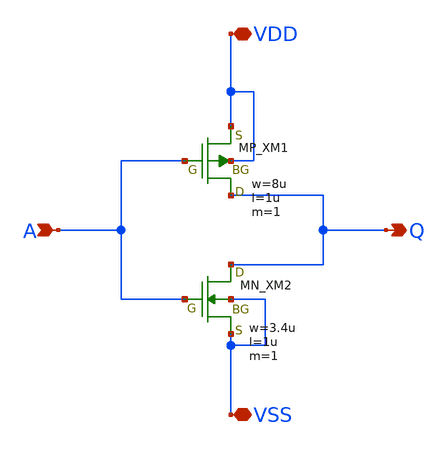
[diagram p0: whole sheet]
** sch_path: inverter/inverter_Tsukasa_Yamamoto.sch
**.subckt inverter_Tsukasa_Yamamoto VDD A Q VSS
*.iopin VDD
*.ipin A
*.opin Q
*.iopin VSS
XXM1 Q A VDD VDD PMOS w=8u l=1u nrd=0 nrs=0 m=1
XXM2 Q A VSS VSS NMOS w=3.4u l=1u nrd=0 nrs=0 m=1
**.ends
.end
